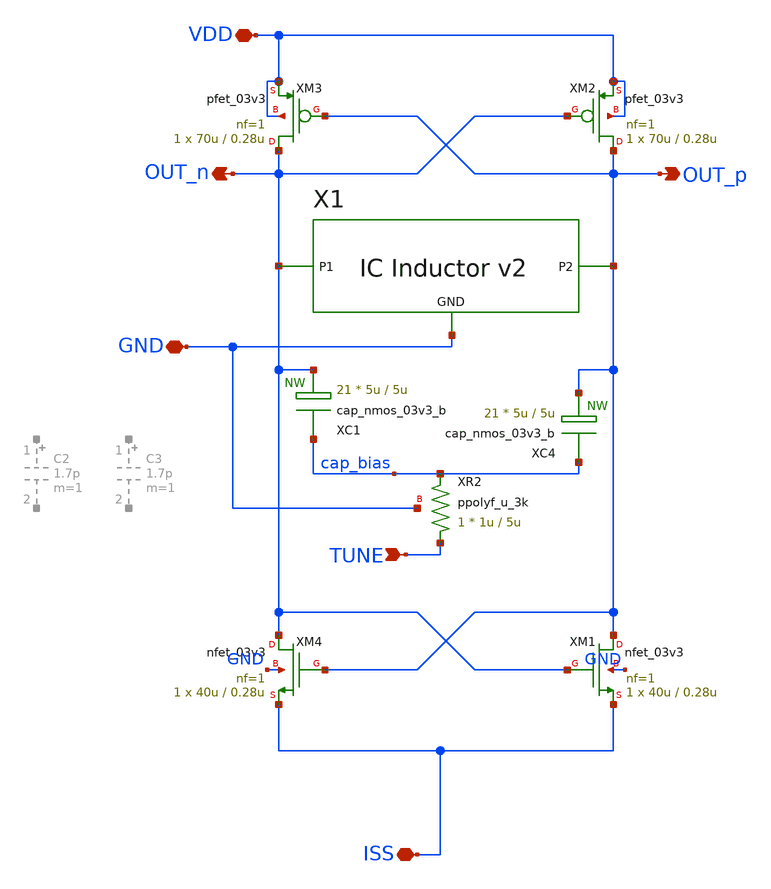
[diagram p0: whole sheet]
** sch_path: team_src/xschem/vco_v1.sch
**.subckt vco_v1 VDD ISS GND TUNE OUT_p OUT_n
*.iopin VDD
*.iopin ISS
*.iopin GND
*.ipin TUNE
*.opin OUT_p
*.opin OUT_n
XM1 OUT_p OUT_n ISS GND nfet_03v3 L=0.28u W=40u nf=1 ad='int((nf+1)/2) * W/nf * 0.18u' as='int((nf+2)/2) * W/nf * 0.18u'
+ pd='2*int((nf+1)/2) * (W/nf + 0.18u)' ps='2*int((nf+2)/2) * (W/nf + 0.18u)' nrd='0.18u / W' nrs='0.18u / W'
+ sa=0 sb=0 sd=0 m=1
XM2 OUT_p OUT_n VDD VDD pfet_03v3 L=0.28u W=70u nf=1 ad='int((nf+1)/2) * W/nf * 0.18u' as='int((nf+2)/2) * W/nf * 0.18u'
+ pd='2*int((nf+1)/2) * (W/nf + 0.18u)' ps='2*int((nf+2)/2) * (W/nf + 0.18u)' nrd='0.18u / W' nrs='0.18u / W'
+ sa=0 sb=0 sd=0 m=1
X1 OUT_n OUT_p GND vco_inductor_v2
XM3 OUT_n OUT_p VDD VDD pfet_03v3 L=0.28u W=70u nf=1 ad='int((nf+1)/2) * W/nf * 0.18u' as='int((nf+2)/2) * W/nf * 0.18u'
+ pd='2*int((nf+1)/2) * (W/nf + 0.18u)' ps='2*int((nf+2)/2) * (W/nf + 0.18u)' nrd='0.18u / W' nrs='0.18u / W'
+ sa=0 sb=0 sd=0 m=1
XM4 OUT_n OUT_p ISS GND nfet_03v3 L=0.28u W=40u nf=1 ad='int((nf+1)/2) * W/nf * 0.18u' as='int((nf+2)/2) * W/nf * 0.18u'
+ pd='2*int((nf+1)/2) * (W/nf + 0.18u)' ps='2*int((nf+2)/2) * (W/nf + 0.18u)' nrd='0.18u / W' nrs='0.18u / W'
+ sa=0 sb=0 sd=0 m=1
XC1 cap_bias OUT_n cap_nmos_03v3_b c_width=5u c_length=5u m=21
XC4 cap_bias OUT_p cap_nmos_03v3_b c_width=5u c_length=5u m=21
XR2 TUNE cap_bias GND ppolyf_u_3k r_width=1u r_length=5u m=1
**.ends

* expanding   symbol:  vco_inductor_v2.sym # of pins=3
** sym_path: team_src/xschem/vco_inductor_v2.sym
.include $UPRJ_ROOT/team_src/xschem/vco_inductor_v2.subckt
.end
